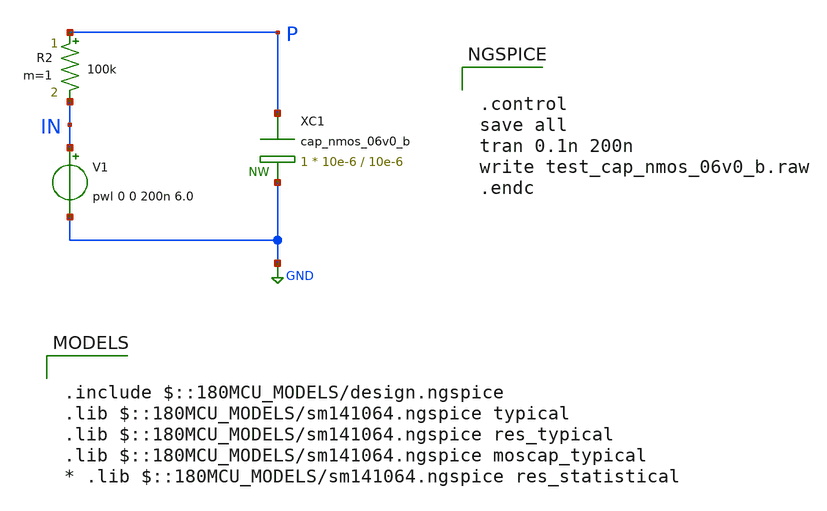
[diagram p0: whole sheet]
** sch_path: gf180mcuD/xschem_libs/gf180mcu_tests/test_cap_nmos_06v0_b/schematic/test_cap_nmos_06v0_b.sch
* Copyright 2022 GlobalFoundries PDK Authors
* Licensed under the Apache License, Version 2.0 (the "License");
* you may not use this file except in compliance with the License.
* You may obtain a copy of the License at
* https://www.apache.org/licenses/LICENSE-2.0
* Unless required by applicable law or agreed to in writing, software
* distributed under the License is distributed on an "AS IS" BASIS,
* WITHOUT WARRANTIES OR CONDITIONS OF ANY KIND, either express or implied.
* See the License for the specific language governing permissions and
* limitations under the License.
**.subckt test_cap_nmos_06v0_b
XC1 P GND cap_nmos_06v0_b c_width=10e-6 c_length=10e-6 m=1
V1 IN GND pwl 0 0 200n 6.0
R2 P IN 100k m=1
**** begin user architecture code

.include $::180MCU_MODELS/design.ngspice
.lib $::180MCU_MODELS/sm141064.ngspice typical
.lib $::180MCU_MODELS/sm141064.ngspice res_typical
.lib $::180MCU_MODELS/sm141064.ngspice moscap_typical
* .lib $::180MCU_MODELS/sm141064.ngspice res_statistical



.control
save all
tran 0.1n 200n
write test_cap_nmos_06v0_b.raw
.endc


**** end user architecture code
**.ends
.GLOBAL GND
.end
